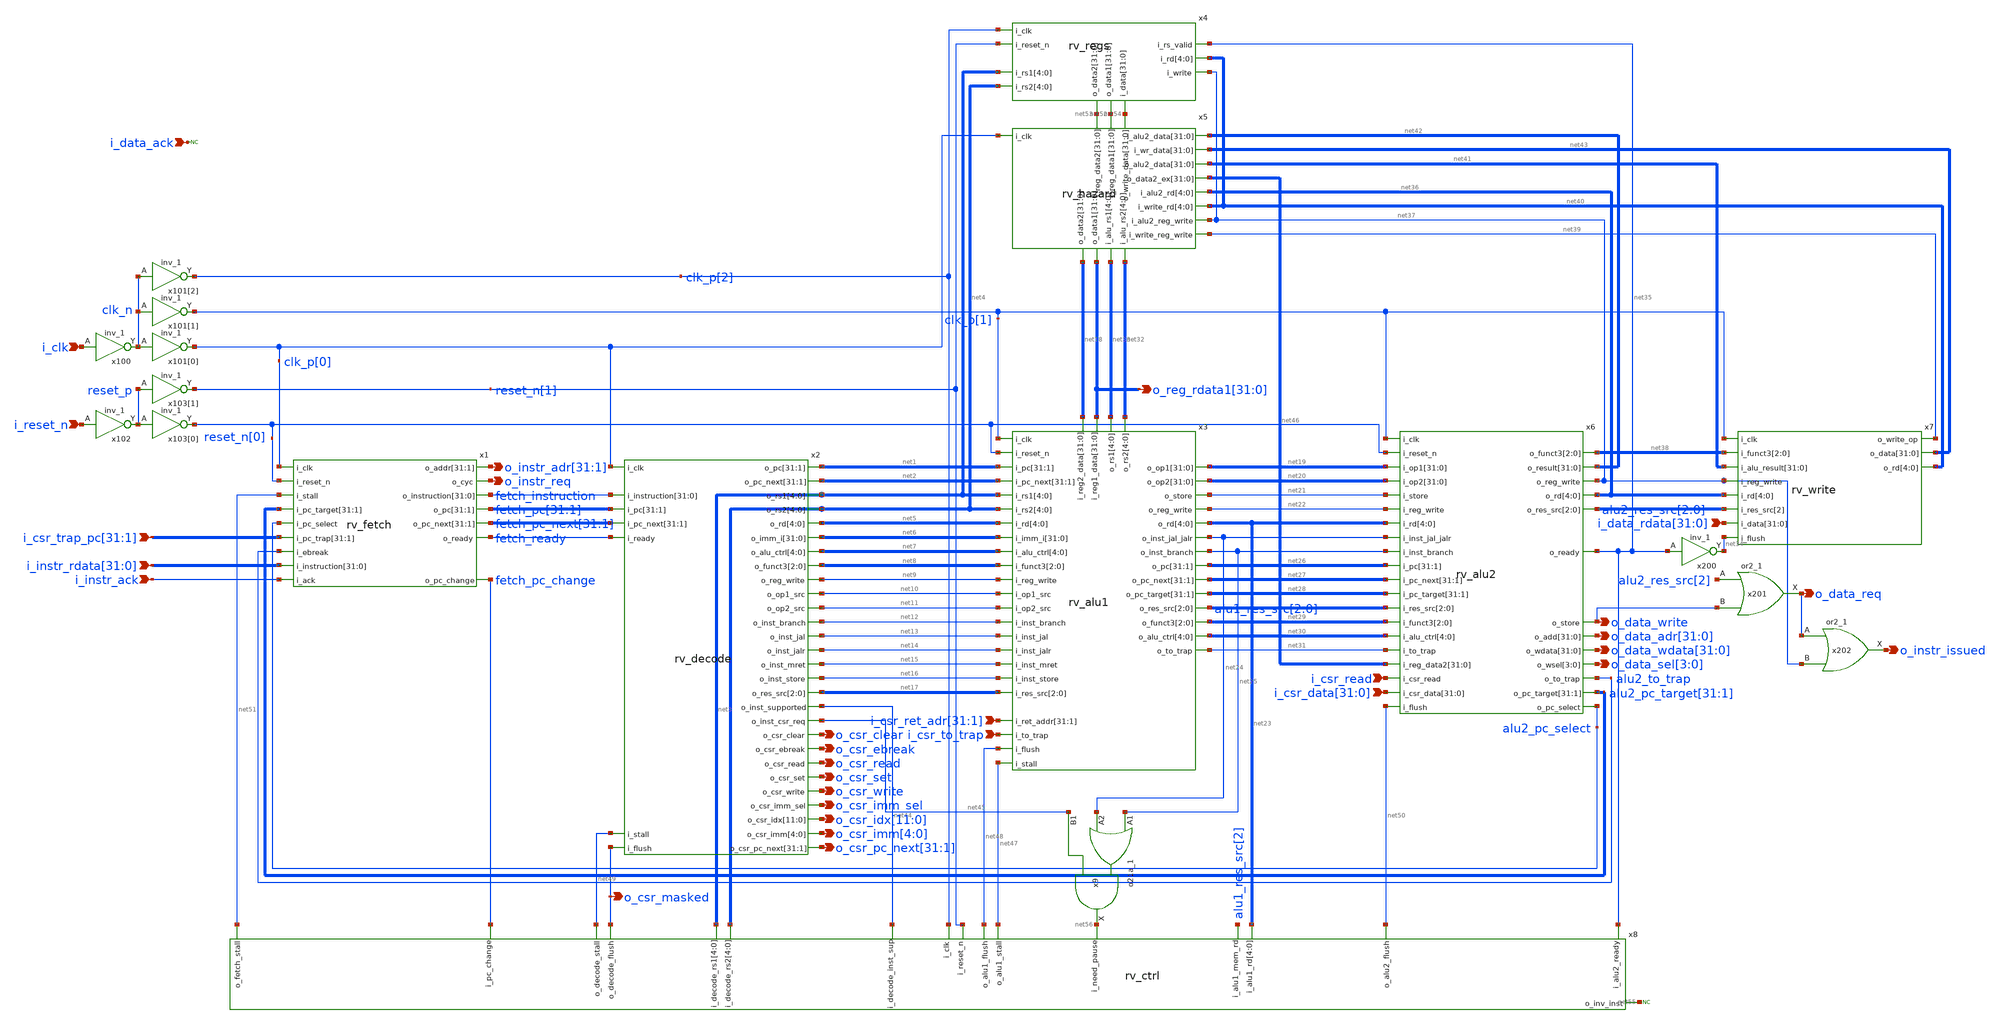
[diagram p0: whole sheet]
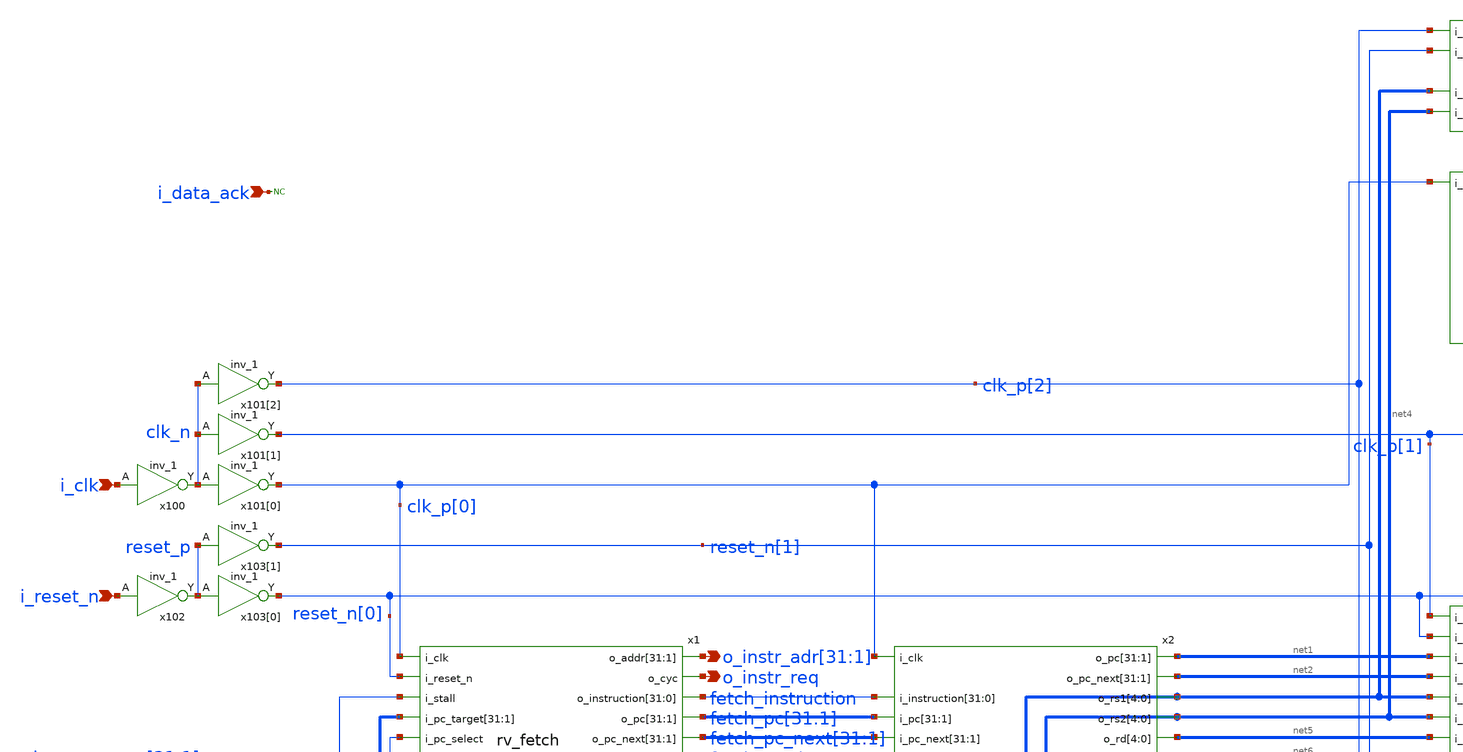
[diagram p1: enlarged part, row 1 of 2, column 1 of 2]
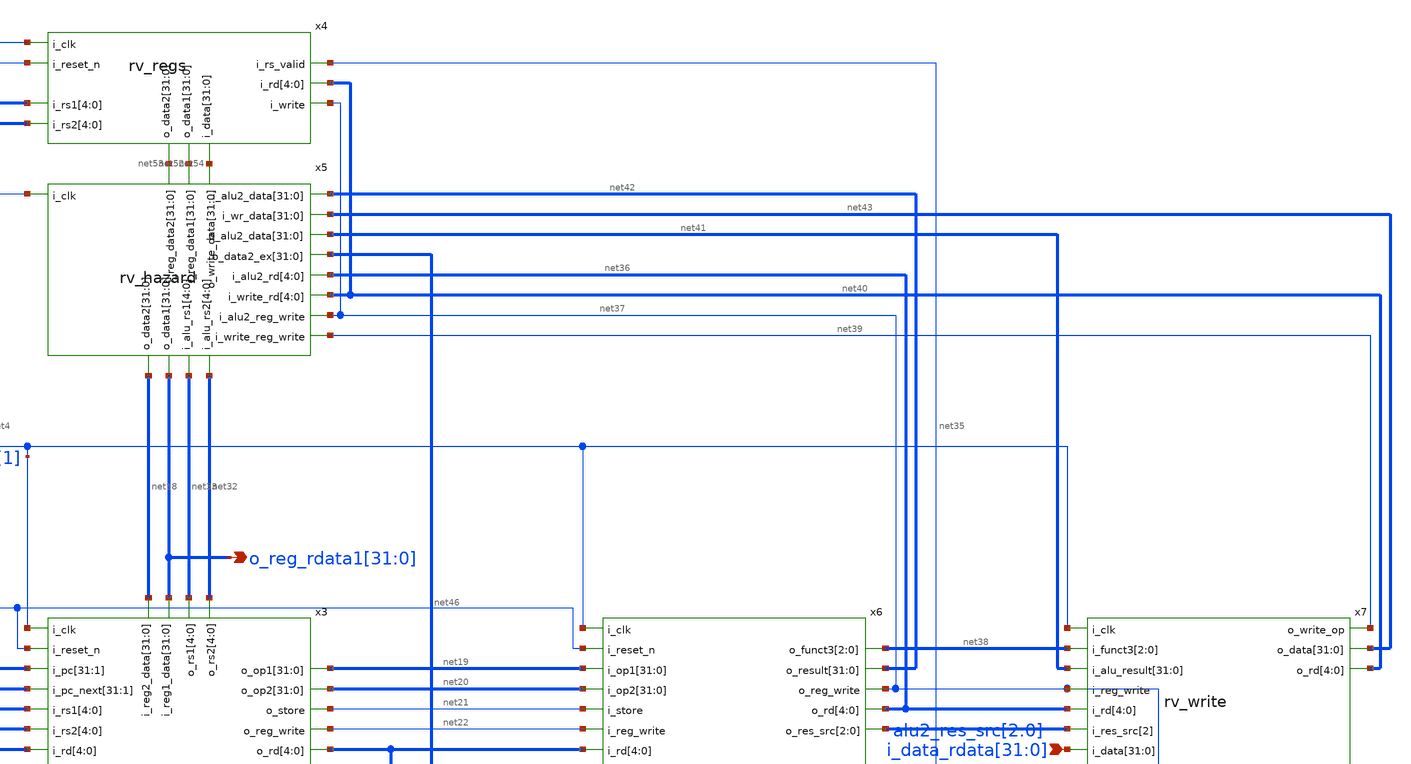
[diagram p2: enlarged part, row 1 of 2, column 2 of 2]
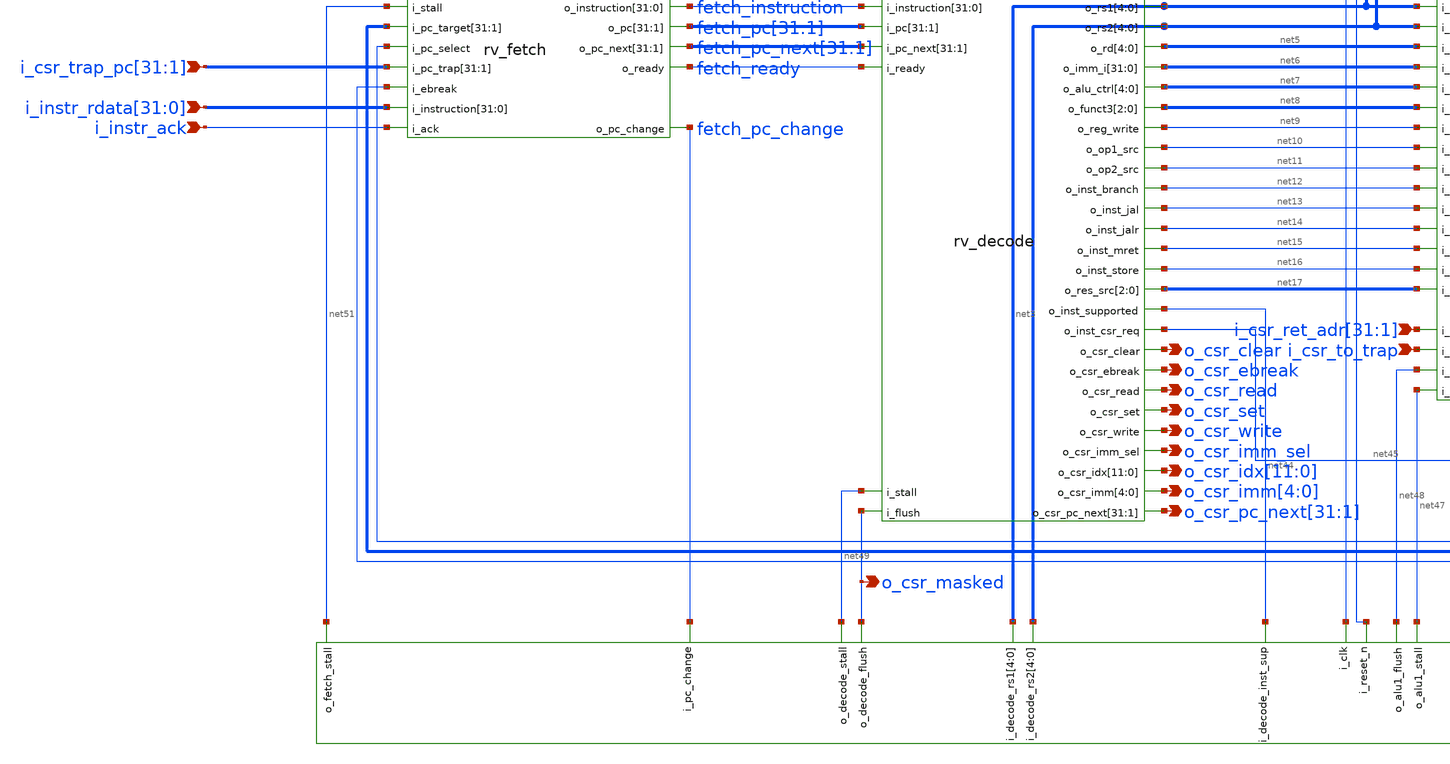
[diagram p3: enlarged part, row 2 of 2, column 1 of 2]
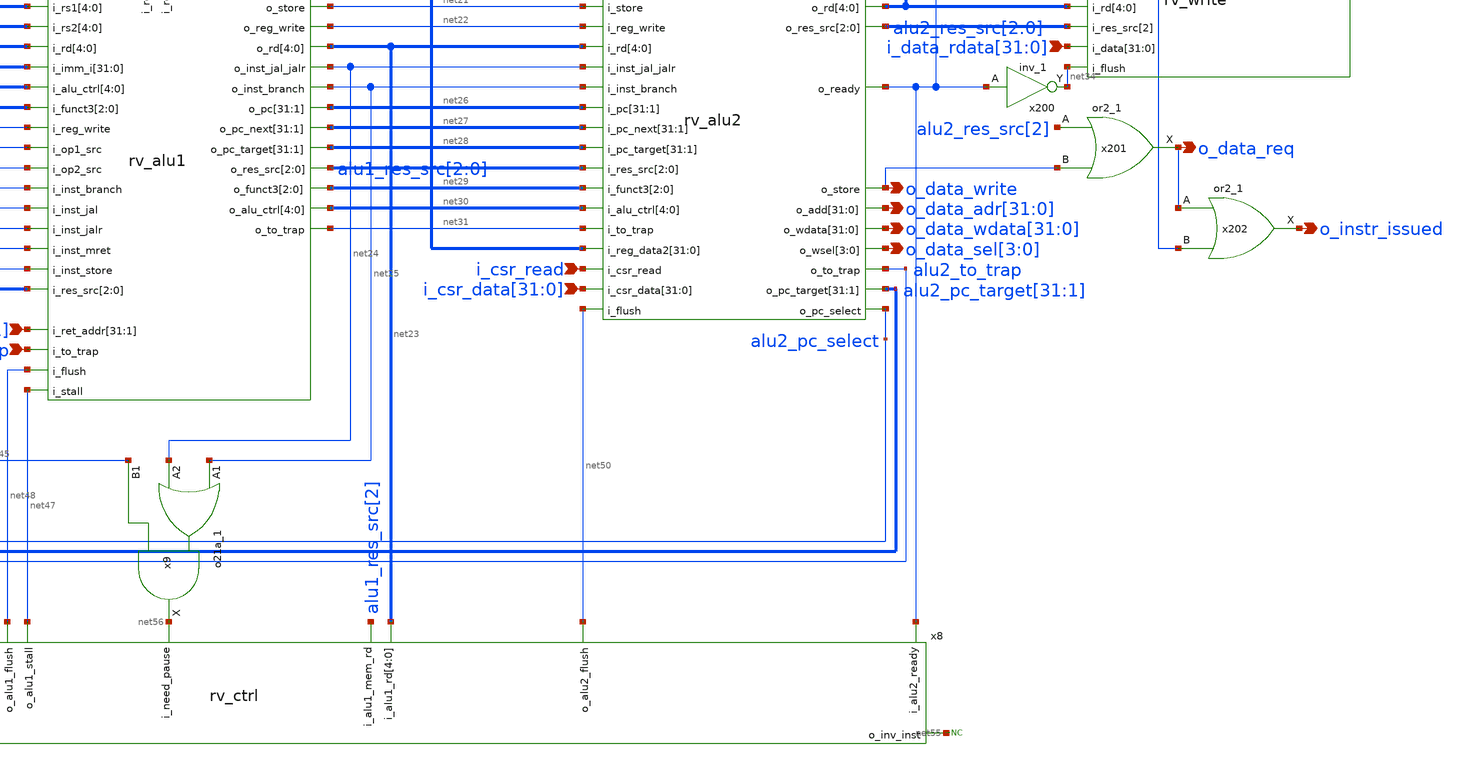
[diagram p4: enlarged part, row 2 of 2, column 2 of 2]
** sch_path: blocks/rv_core/rv_core.sch
**.subckt rv_core i_clk i_reset_n i_csr_read o_csr_clear o_data_req
*+ o_data_wdata[31],o_data_wdata[30],o_data_wdata[29],o_data_wdata[28],o_data_wdata[27],o_data_wdata[26],o_data_wdata[25],o_data_wdata[24],o_data_wdata[23],o_data_wdata[22],o_data_wdata[21],o_data_wdata[20],o_data_wdata[19],o_data_wdata[18],o_data_wdata[17],o_data_wdata[16],o_data_wdata[15],o_data_wdata[14],o_data_wdata[13],o_data_wdata[12],o_data_wdata[11],o_data_wdata[10],o_data_wdata[9],o_data_wdata[8],o_data_wdata[7],o_data_wdata[6],o_data_wdata[5],o_data_wdata[4],o_data_wdata[3],o_data_wdata[2],o_data_wdata[1],o_data_wdata[0] o_instr_issued
*+ o_data_adr[31],o_data_adr[30],o_data_adr[29],o_data_adr[28],o_data_adr[27],o_data_adr[26],o_data_adr[25],o_data_adr[24],o_data_adr[23],o_data_adr[22],o_data_adr[21],o_data_adr[20],o_data_adr[19],o_data_adr[18],o_data_adr[17],o_data_adr[16],o_data_adr[15],o_data_adr[14],o_data_adr[13],o_data_adr[12],o_data_adr[11],o_data_adr[10],o_data_adr[9],o_data_adr[8],o_data_adr[7],o_data_adr[6],o_data_adr[5],o_data_adr[4],o_data_adr[3],o_data_adr[2],o_data_adr[1],o_data_adr[0] o_data_sel[3],o_data_sel[2],o_data_sel[1],o_data_sel[0]
*+ i_csr_data[31],i_csr_data[30],i_csr_data[29],i_csr_data[28],i_csr_data[27],i_csr_data[26],i_csr_data[25],i_csr_data[24],i_csr_data[23],i_csr_data[22],i_csr_data[21],i_csr_data[20],i_csr_data[19],i_csr_data[18],i_csr_data[17],i_csr_data[16],i_csr_data[15],i_csr_data[14],i_csr_data[13],i_csr_data[12],i_csr_data[11],i_csr_data[10],i_csr_data[9],i_csr_data[8],i_csr_data[7],i_csr_data[6],i_csr_data[5],i_csr_data[4],i_csr_data[3],i_csr_data[2],i_csr_data[1],i_csr_data[0] i_csr_to_trap o_csr_ebreak o_csr_read o_csr_set o_csr_write o_csr_imm_sel
*+ i_csr_ret_adr[31],i_csr_ret_adr[30],i_csr_ret_adr[29],i_csr_ret_adr[28],i_csr_ret_adr[27],i_csr_ret_adr[26],i_csr_ret_adr[25],i_csr_ret_adr[24],i_csr_ret_adr[23],i_csr_ret_adr[22],i_csr_ret_adr[21],i_csr_ret_adr[20],i_csr_ret_adr[19],i_csr_ret_adr[18],i_csr_ret_adr[17],i_csr_ret_adr[16],i_csr_ret_adr[15],i_csr_ret_adr[14],i_csr_ret_adr[13],i_csr_ret_adr[12],i_csr_ret_adr[11],i_csr_ret_adr[10],i_csr_ret_adr[9],i_csr_ret_adr[8],i_csr_ret_adr[7],i_csr_ret_adr[6],i_csr_ret_adr[5],i_csr_ret_adr[4],i_csr_ret_adr[3],i_csr_ret_adr[2],i_csr_ret_adr[1]
*+ i_csr_trap_pc[31],i_csr_trap_pc[30],i_csr_trap_pc[29],i_csr_trap_pc[28],i_csr_trap_pc[27],i_csr_trap_pc[26],i_csr_trap_pc[25],i_csr_trap_pc[24],i_csr_trap_pc[23],i_csr_trap_pc[22],i_csr_trap_pc[21],i_csr_trap_pc[20],i_csr_trap_pc[19],i_csr_trap_pc[18],i_csr_trap_pc[17],i_csr_trap_pc[16],i_csr_trap_pc[15],i_csr_trap_pc[14],i_csr_trap_pc[13],i_csr_trap_pc[12],i_csr_trap_pc[11],i_csr_trap_pc[10],i_csr_trap_pc[9],i_csr_trap_pc[8],i_csr_trap_pc[7],i_csr_trap_pc[6],i_csr_trap_pc[5],i_csr_trap_pc[4],i_csr_trap_pc[3],i_csr_trap_pc[2],i_csr_trap_pc[1]
*+ o_csr_idx[11],o_csr_idx[10],o_csr_idx[9],o_csr_idx[8],o_csr_idx[7],o_csr_idx[6],o_csr_idx[5],o_csr_idx[4],o_csr_idx[3],o_csr_idx[2],o_csr_idx[1],o_csr_idx[0] o_csr_imm[4],o_csr_imm[3],o_csr_imm[2],o_csr_imm[1],o_csr_imm[0]
*+ o_csr_pc_next[31],o_csr_pc_next[30],o_csr_pc_next[29],o_csr_pc_next[28],o_csr_pc_next[27],o_csr_pc_next[26],o_csr_pc_next[25],o_csr_pc_next[24],o_csr_pc_next[23],o_csr_pc_next[22],o_csr_pc_next[21],o_csr_pc_next[20],o_csr_pc_next[19],o_csr_pc_next[18],o_csr_pc_next[17],o_csr_pc_next[16],o_csr_pc_next[15],o_csr_pc_next[14],o_csr_pc_next[13],o_csr_pc_next[12],o_csr_pc_next[11],o_csr_pc_next[10],o_csr_pc_next[9],o_csr_pc_next[8],o_csr_pc_next[7],o_csr_pc_next[6],o_csr_pc_next[5],o_csr_pc_next[4],o_csr_pc_next[3],o_csr_pc_next[2],o_csr_pc_next[1]
*+ o_reg_rdata1[31],o_reg_rdata1[30],o_reg_rdata1[29],o_reg_rdata1[28],o_reg_rdata1[27],o_reg_rdata1[26],o_reg_rdata1[25],o_reg_rdata1[24],o_reg_rdata1[23],o_reg_rdata1[22],o_reg_rdata1[21],o_reg_rdata1[20],o_reg_rdata1[19],o_reg_rdata1[18],o_reg_rdata1[17],o_reg_rdata1[16],o_reg_rdata1[15],o_reg_rdata1[14],o_reg_rdata1[13],o_reg_rdata1[12],o_reg_rdata1[11],o_reg_rdata1[10],o_reg_rdata1[9],o_reg_rdata1[8],o_reg_rdata1[7],o_reg_rdata1[6],o_reg_rdata1[5],o_reg_rdata1[4],o_reg_rdata1[3],o_reg_rdata1[2],o_reg_rdata1[1],o_reg_rdata1[0] i_data_ack o_data_write
*+ i_data_rdata[31],i_data_rdata[30],i_data_rdata[29],i_data_rdata[28],i_data_rdata[27],i_data_rdata[26],i_data_rdata[25],i_data_rdata[24],i_data_rdata[23],i_data_rdata[22],i_data_rdata[21],i_data_rdata[20],i_data_rdata[19],i_data_rdata[18],i_data_rdata[17],i_data_rdata[16],i_data_rdata[15],i_data_rdata[14],i_data_rdata[13],i_data_rdata[12],i_data_rdata[11],i_data_rdata[10],i_data_rdata[9],i_data_rdata[8],i_data_rdata[7],i_data_rdata[6],i_data_rdata[5],i_data_rdata[4],i_data_rdata[3],i_data_rdata[2],i_data_rdata[1],i_data_rdata[0] i_instr_ack o_instr_req
*+ i_instr_rdata[31],i_instr_rdata[30],i_instr_rdata[29],i_instr_rdata[28],i_instr_rdata[27],i_instr_rdata[26],i_instr_rdata[25],i_instr_rdata[24],i_instr_rdata[23],i_instr_rdata[22],i_instr_rdata[21],i_instr_rdata[20],i_instr_rdata[19],i_instr_rdata[18],i_instr_rdata[17],i_instr_rdata[16],i_instr_rdata[15],i_instr_rdata[14],i_instr_rdata[13],i_instr_rdata[12],i_instr_rdata[11],i_instr_rdata[10],i_instr_rdata[9],i_instr_rdata[8],i_instr_rdata[7],i_instr_rdata[6],i_instr_rdata[5],i_instr_rdata[4],i_instr_rdata[3],i_instr_rdata[2],i_instr_rdata[1],i_instr_rdata[0]
*+ o_instr_adr[31],o_instr_adr[30],o_instr_adr[29],o_instr_adr[28],o_instr_adr[27],o_instr_adr[26],o_instr_adr[25],o_instr_adr[24],o_instr_adr[23],o_instr_adr[22],o_instr_adr[21],o_instr_adr[20],o_instr_adr[19],o_instr_adr[18],o_instr_adr[17],o_instr_adr[16],o_instr_adr[15],o_instr_adr[14],o_instr_adr[13],o_instr_adr[12],o_instr_adr[11],o_instr_adr[10],o_instr_adr[9],o_instr_adr[8],o_instr_adr[7],o_instr_adr[6],o_instr_adr[5],o_instr_adr[4],o_instr_adr[3],o_instr_adr[2],o_instr_adr[1] o_csr_masked
*.ipin i_clk
*.ipin i_reset_n
*.ipin i_csr_read
*.opin o_csr_clear
*.opin o_data_req
*.opin
*+ o_data_wdata[31],o_data_wdata[30],o_data_wdata[29],o_data_wdata[28],o_data_wdata[27],o_data_wdata[26],o_data_wdata[25],o_data_wdata[24],o_data_wdata[23],o_data_wdata[22],o_data_wdata[21],o_data_wdata[20],o_data_wdata[19],o_data_wdata[18],o_data_wdata[17],o_data_wdata[16],o_data_wdata[15],o_data_wdata[14],o_data_wdata[13],o_data_wdata[12],o_data_wdata[11],o_data_wdata[10],o_data_wdata[9],o_data_wdata[8],o_data_wdata[7],o_data_wdata[6],o_data_wdata[5],o_data_wdata[4],o_data_wdata[3],o_data_wdata[2],o_data_wdata[1],o_data_wdata[0]
*.opin o_instr_issued
*.opin
*+ o_data_adr[31],o_data_adr[30],o_data_adr[29],o_data_adr[28],o_data_adr[27],o_data_adr[26],o_data_adr[25],o_data_adr[24],o_data_adr[23],o_data_adr[22],o_data_adr[21],o_data_adr[20],o_data_adr[19],o_data_adr[18],o_data_adr[17],o_data_adr[16],o_data_adr[15],o_data_adr[14],o_data_adr[13],o_data_adr[12],o_data_adr[11],o_data_adr[10],o_data_adr[9],o_data_adr[8],o_data_adr[7],o_data_adr[6],o_data_adr[5],o_data_adr[4],o_data_adr[3],o_data_adr[2],o_data_adr[1],o_data_adr[0]
*.opin o_data_sel[3],o_data_sel[2],o_data_sel[1],o_data_sel[0]
*.ipin
*+ i_csr_data[31],i_csr_data[30],i_csr_data[29],i_csr_data[28],i_csr_data[27],i_csr_data[26],i_csr_data[25],i_csr_data[24],i_csr_data[23],i_csr_data[22],i_csr_data[21],i_csr_data[20],i_csr_data[19],i_csr_data[18],i_csr_data[17],i_csr_data[16],i_csr_data[15],i_csr_data[14],i_csr_data[13],i_csr_data[12],i_csr_data[11],i_csr_data[10],i_csr_data[9],i_csr_data[8],i_csr_data[7],i_csr_data[6],i_csr_data[5],i_csr_data[4],i_csr_data[3],i_csr_data[2],i_csr_data[1],i_csr_data[0]
*.ipin i_csr_to_trap
*.opin o_csr_ebreak
*.opin o_csr_read
*.opin o_csr_set
*.opin o_csr_write
*.opin o_csr_imm_sel
*.ipin
*+ i_csr_ret_adr[31],i_csr_ret_adr[30],i_csr_ret_adr[29],i_csr_ret_adr[28],i_csr_ret_adr[27],i_csr_ret_adr[26],i_csr_ret_adr[25],i_csr_ret_adr[24],i_csr_ret_adr[23],i_csr_ret_adr[22],i_csr_ret_adr[21],i_csr_ret_adr[20],i_csr_ret_adr[19],i_csr_ret_adr[18],i_csr_ret_adr[17],i_csr_ret_adr[16],i_csr_ret_adr[15],i_csr_ret_adr[14],i_csr_ret_adr[13],i_csr_ret_adr[12],i_csr_ret_adr[11],i_csr_ret_adr[10],i_csr_ret_adr[9],i_csr_ret_adr[8],i_csr_ret_adr[7],i_csr_ret_adr[6],i_csr_ret_adr[5],i_csr_ret_adr[4],i_csr_ret_adr[3],i_csr_ret_adr[2],i_csr_ret_adr[1]
*.ipin
*+ i_csr_trap_pc[31],i_csr_trap_pc[30],i_csr_trap_pc[29],i_csr_trap_pc[28],i_csr_trap_pc[27],i_csr_trap_pc[26],i_csr_trap_pc[25],i_csr_trap_pc[24],i_csr_trap_pc[23],i_csr_trap_pc[22],i_csr_trap_pc[21],i_csr_trap_pc[20],i_csr_trap_pc[19],i_csr_trap_pc[18],i_csr_trap_pc[17],i_csr_trap_pc[16],i_csr_trap_pc[15],i_csr_trap_pc[14],i_csr_trap_pc[13],i_csr_trap_pc[12],i_csr_trap_pc[11],i_csr_trap_pc[10],i_csr_trap_pc[9],i_csr_trap_pc[8],i_csr_trap_pc[7],i_csr_trap_pc[6],i_csr_trap_pc[5],i_csr_trap_pc[4],i_csr_trap_pc[3],i_csr_trap_pc[2],i_csr_trap_pc[1]
*.opin
*+ o_csr_idx[11],o_csr_idx[10],o_csr_idx[9],o_csr_idx[8],o_csr_idx[7],o_csr_idx[6],o_csr_idx[5],o_csr_idx[4],o_csr_idx[3],o_csr_idx[2],o_csr_idx[1],o_csr_idx[0]
*.opin o_csr_imm[4],o_csr_imm[3],o_csr_imm[2],o_csr_imm[1],o_csr_imm[0]
*.opin
*+ o_csr_pc_next[31],o_csr_pc_next[30],o_csr_pc_next[29],o_csr_pc_next[28],o_csr_pc_next[27],o_csr_pc_next[26],o_csr_pc_next[25],o_csr_pc_next[24],o_csr_pc_next[23],o_csr_pc_next[22],o_csr_pc_next[21],o_csr_pc_next[20],o_csr_pc_next[19],o_csr_pc_next[18],o_csr_pc_next[17],o_csr_pc_next[16],o_csr_pc_next[15],o_csr_pc_next[14],o_csr_pc_next[13],o_csr_pc_next[12],o_csr_pc_next[11],o_csr_pc_next[10],o_csr_pc_next[9],o_csr_pc_next[8],o_csr_pc_next[7],o_csr_pc_next[6],o_csr_pc_next[5],o_csr_pc_next[4],o_csr_pc_next[3],o_csr_pc_next[2],o_csr_pc_next[1]
*.opin
*+ o_reg_rdata1[31],o_reg_rdata1[30],o_reg_rdata1[29],o_reg_rdata1[28],o_reg_rdata1[27],o_reg_rdata1[26],o_reg_rdata1[25],o_reg_rdata1[24],o_reg_rdata1[23],o_reg_rdata1[22],o_reg_rdata1[21],o_reg_rdata1[20],o_reg_rdata1[19],o_reg_rdata1[18],o_reg_rdata1[17],o_reg_rdata1[16],o_reg_rdata1[15],o_reg_rdata1[14],o_reg_rdata1[13],o_reg_rdata1[12],o_reg_rdata1[11],o_reg_rdata1[10],o_reg_rdata1[9],o_reg_rdata1[8],o_reg_rdata1[7],o_reg_rdata1[6],o_reg_rdata1[5],o_reg_rdata1[4],o_reg_rdata1[3],o_reg_rdata1[2],o_reg_rdata1[1],o_reg_rdata1[0]
*.ipin i_data_ack
*.opin o_data_write
*.ipin
*+ i_data_rdata[31],i_data_rdata[30],i_data_rdata[29],i_data_rdata[28],i_data_rdata[27],i_data_rdata[26],i_data_rdata[25],i_data_rdata[24],i_data_rdata[23],i_data_rdata[22],i_data_rdata[21],i_data_rdata[20],i_data_rdata[19],i_data_rdata[18],i_data_rdata[17],i_data_rdata[16],i_data_rdata[15],i_data_rdata[14],i_data_rdata[13],i_data_rdata[12],i_data_rdata[11],i_data_rdata[10],i_data_rdata[9],i_data_rdata[8],i_data_rdata[7],i_data_rdata[6],i_data_rdata[5],i_data_rdata[4],i_data_rdata[3],i_data_rdata[2],i_data_rdata[1],i_data_rdata[0]
*.ipin i_instr_ack
*.opin o_instr_req
*.ipin
*+ i_instr_rdata[31],i_instr_rdata[30],i_instr_rdata[29],i_instr_rdata[28],i_instr_rdata[27],i_instr_rdata[26],i_instr_rdata[25],i_instr_rdata[24],i_instr_rdata[23],i_instr_rdata[22],i_instr_rdata[21],i_instr_rdata[20],i_instr_rdata[19],i_instr_rdata[18],i_instr_rdata[17],i_instr_rdata[16],i_instr_rdata[15],i_instr_rdata[14],i_instr_rdata[13],i_instr_rdata[12],i_instr_rdata[11],i_instr_rdata[10],i_instr_rdata[9],i_instr_rdata[8],i_instr_rdata[7],i_instr_rdata[6],i_instr_rdata[5],i_instr_rdata[4],i_instr_rdata[3],i_instr_rdata[2],i_instr_rdata[1],i_instr_rdata[0]
*.opin
*+ o_instr_adr[31],o_instr_adr[30],o_instr_adr[29],o_instr_adr[28],o_instr_adr[27],o_instr_adr[26],o_instr_adr[25],o_instr_adr[24],o_instr_adr[23],o_instr_adr[22],o_instr_adr[21],o_instr_adr[20],o_instr_adr[19],o_instr_adr[18],o_instr_adr[17],o_instr_adr[16],o_instr_adr[15],o_instr_adr[14],o_instr_adr[13],o_instr_adr[12],o_instr_adr[11],o_instr_adr[10],o_instr_adr[9],o_instr_adr[8],o_instr_adr[7],o_instr_adr[6],o_instr_adr[5],o_instr_adr[4],o_instr_adr[3],o_instr_adr[2],o_instr_adr[1]
*.opin o_csr_masked
x1 fetch_pc_change clk_p[0] reset_n[0] o_instr_adr[31] o_instr_adr[30] o_instr_adr[29]
+ o_instr_adr[28] o_instr_adr[27] o_instr_adr[26] o_instr_adr[25] o_instr_adr[24] o_instr_adr[23] o_instr_adr[22]
+ o_instr_adr[21] o_instr_adr[20] o_instr_adr[19] o_instr_adr[18] o_instr_adr[17] o_instr_adr[16] o_instr_adr[15]
+ o_instr_adr[14] o_instr_adr[13] o_instr_adr[12] o_instr_adr[11] o_instr_adr[10] o_instr_adr[9] o_instr_adr[8]
+ o_instr_adr[7] o_instr_adr[6] o_instr_adr[5] o_instr_adr[4] o_instr_adr[3] o_instr_adr[2] o_instr_adr[1]
+ o_instr_req net51 fetch_instruction fetch_instruction fetch_instruction fetch_instruction fetch_instruction
+ fetch_instruction fetch_instruction fetch_instruction fetch_instruction fetch_instruction fetch_instruction
+ fetch_instruction fetch_instruction fetch_instruction fetch_instruction fetch_instruction fetch_instruction
+ fetch_instruction fetch_instruction fetch_instruction fetch_instruction fetch_instruction fetch_instruction
+ fetch_instruction fetch_instruction fetch_instruction fetch_instruction fetch_instruction fetch_instruction
+ fetch_instruction fetch_instruction fetch_instruction alu2_pc_target[31] alu2_pc_target[30] alu2_pc_target[29]
+ alu2_pc_target[28] alu2_pc_target[27] alu2_pc_target[26] alu2_pc_target[25] alu2_pc_target[24] alu2_pc_target[23]
+ alu2_pc_target[22] alu2_pc_target[21] alu2_pc_target[20] alu2_pc_target[19] alu2_pc_target[18] alu2_pc_target[17]
+ alu2_pc_target[16] alu2_pc_target[15] alu2_pc_target[14] alu2_pc_target[13] alu2_pc_target[12] alu2_pc_target[11]
+ alu2_pc_target[10] alu2_pc_target[9] alu2_pc_target[8] alu2_pc_target[7] alu2_pc_target[6] alu2_pc_target[5]
+ alu2_pc_target[4] alu2_pc_target[3] alu2_pc_target[2] alu2_pc_target[1] alu2_pc_select fetch_pc[31] fetch_pc[30]
+ fetch_pc[29] fetch_pc[28] fetch_pc[27] fetch_pc[26] fetch_pc[25] fetch_pc[24] fetch_pc[23] fetch_pc[22]
+ fetch_pc[21] fetch_pc[20] fetch_pc[19] fetch_pc[18] fetch_pc[17] fetch_pc[16] fetch_pc[15] fetch_pc[14]
+ fetch_pc[13] fetch_pc[12] fetch_pc[11] fetch_pc[10] fetch_pc[9] fetch_pc[8] fetch_pc[7] fetch_pc[6] fetch_pc[5]
+ fetch_pc[4] fetch_pc[3] fetch_pc[2] fetch_pc[1] fetch_pc_next[31] fetch_pc_next[30] fetch_pc_next[29]
+ fetch_pc_next[28] fetch_pc_next[27] fetch_pc_next[26] fetch_pc_next[25] fetch_pc_next[24] fetch_pc_next[23]
+ fetch_pc_next[22] fetch_pc_next[21] fetch_pc_next[20] fetch_pc_next[19] fetch_pc_next[18] fetch_pc_next[17]
+ fetch_pc_next[16] fetch_pc_next[15] fetch_pc_next[14] fetch_pc_next[13] fetch_pc_next[12] fetch_pc_next[11]
+ fetch_pc_next[10] fetch_pc_next[9] fetch_pc_next[8] fetch_pc_next[7] fetch_pc_next[6] fetch_pc_next[5]
+ fetch_pc_next[4] fetch_pc_next[3] fetch_pc_next[2] fetch_pc_next[1] i_csr_trap_pc[31] i_csr_trap_pc[30]
+ i_csr_trap_pc[29] i_csr_trap_pc[28] i_csr_trap_pc[27] i_csr_trap_pc[26] i_csr_trap_pc[25] i_csr_trap_pc[24]
+ i_csr_trap_pc[23] i_csr_trap_pc[22] i_csr_trap_pc[21] i_csr_trap_pc[20] i_csr_trap_pc[19] i_csr_trap_pc[18]
+ i_csr_trap_pc[17] i_csr_trap_pc[16] i_csr_trap_pc[15] i_csr_trap_pc[14] i_csr_trap_pc[13] i_csr_trap_pc[12]
+ i_csr_trap_pc[11] i_csr_trap_pc[10] i_csr_trap_pc[9] i_csr_trap_pc[8] i_csr_trap_pc[7] i_csr_trap_pc[6]
+ i_csr_trap_pc[5] i_csr_trap_pc[4] i_csr_trap_pc[3] i_csr_trap_pc[2] i_csr_trap_pc[1] fetch_ready alu2_to_trap
+ i_instr_rdata[31] i_instr_rdata[30] i_instr_rdata[29] i_instr_rdata[28] i_instr_rdata[27] i_instr_rdata[26]
+ i_instr_rdata[25] i_instr_rdata[24] i_instr_rdata[23] i_instr_rdata[22] i_instr_rdata[21] i_instr_rdata[20]
+ i_instr_rdata[19] i_instr_rdata[18] i_instr_rdata[17] i_instr_rdata[16] i_instr_rdata[15] i_instr_rdata[14]
+ i_instr_rdata[13] i_instr_rdata[12] i_instr_rdata[11] i_instr_rdata[10] i_instr_rdata[9] i_instr_rdata[8]
+ i_instr_rdata[7] i_instr_rdata[6] i_instr_rdata[5] i_instr_rdata[4] i_instr_rdata[3] i_instr_rdata[2]
+ i_instr_rdata[1] i_instr_rdata[0] i_instr_ack rv_fetch
x100 i_clk VSS VSS VCC VCC clk_n sky130_fd_sc_hs__inv_1
x102 i_reset_n VSS VSS VCC VCC reset_p sky130_fd_sc_hs__inv_1
x103[0] reset_p VSS VSS VCC VCC reset_n[0] sky130_fd_sc_hs__inv_1
x101[2] clk_n VSS VSS VCC VCC clk_p[2] sky130_fd_sc_hs__inv_1
x101[1] clk_n VSS VSS VCC VCC clk_p[1] sky130_fd_sc_hs__inv_1
x101[0] clk_n VSS VSS VCC VCC clk_p[0] sky130_fd_sc_hs__inv_1
x103[1] reset_p VSS VSS VCC VCC reset_n[1] sky130_fd_sc_hs__inv_1
x2 net1[30] net1[29] net1[28] net1[27] net1[26] net1[25] net1[24] net1[23] net1[22] net1[21]
+ net1[20] net1[19] net1[18] net1[17] net1[16] net1[15] net1[14] net1[13] net1[12] net1[11] net1[10] net1[9]
+ net1[8] net1[7] net1[6] net1[5] net1[4] net1[3] net1[2] net1[1] net1[0] clk_p[0] net49 net2[30] net2[29]
+ net2[28] net2[27] net2[26] net2[25] net2[24] net2[23] net2[22] net2[21] net2[20] net2[19] net2[18] net2[17]
+ net2[16] net2[15] net2[14] net2[13] net2[12] net2[11] net2[10] net2[9] net2[8] net2[7] net2[6] net2[5]
+ net2[4] net2[3] net2[2] net2[1] net2[0] o_csr_masked net3[4] net3[3] net3[2] net3[1] net3[0]
+ fetch_instruction fetch_instruction fetch_instruction fetch_instruction fetch_instruction fetch_instruction
+ fetch_instruction fetch_instruction fetch_instruction fetch_instruction fetch_instruction fetch_instruction
+ fetch_instruction fetch_instruction fetch_instruction fetch_instruction fetch_instruction fetch_instruction
+ fetch_instruction fetch_instruction fetch_instruction fetch_instruction fetch_instruction fetch_instruction
+ fetch_instruction fetch_instruction fetch_instruction fetch_instruction fetch_instruction fetch_instruction
+ fetch_instruction fetch_instruction net4[4] net4[3] net4[2] net4[1] net4[0] net5[4] net5[3] net5[2] net5[1] net5[0]
+ fetch_pc[31] fetch_pc[30] fetch_pc[29] fetch_pc[28] fetch_pc[27] fetch_pc[26] fetch_pc[25] fetch_pc[24]
+ fetch_pc[23] fetch_pc[22] fetch_pc[21] fetch_pc[20] fetch_pc[19] fetch_pc[18] fetch_pc[17] fetch_pc[16]
+ fetch_pc[15] fetch_pc[14] fetch_pc[13] fetch_pc[12] fetch_pc[11] fetch_pc[10] fetch_pc[9] fetch_pc[8]
+ fetch_pc[7] fetch_pc[6] fetch_pc[5] fetch_pc[4] fetch_pc[3] fetch_pc[2] fetch_pc[1] net6[31] net6[30] net6[29]
+ net6[28] net6[27] net6[26] net6[25] net6[24] net6[23] net6[22] net6[21] net6[20] net6[19] net6[18] net6[17]
+ net6[16] net6[15] net6[14] net6[13] net6[12] net6[11] net6[10] net6[9] net6[8] net6[7] net6[6] net6[5]
+ net6[4] net6[3] net6[2] net6[1] net6[0] fetch_pc_next[31] fetch_pc_next[30] fetch_pc_next[29]
+ fetch_pc_next[28] fetch_pc_next[27] fetch_pc_next[26] fetch_pc_next[25] fetch_pc_next[24] fetch_pc_next[23]
+ fetch_pc_next[22] fetch_pc_next[21] fetch_pc_next[20] fetch_pc_next[19] fetch_pc_next[18] fetch_pc_next[17]
+ fetch_pc_next[16] fetch_pc_next[15] fetch_pc_next[14] fetch_pc_next[13] fetch_pc_next[12] fetch_pc_next[11]
+ fetch_pc_next[10] fetch_pc_next[9] fetch_pc_next[8] fetch_pc_next[7] fetch_pc_next[6] fetch_pc_next[5]
+ fetch_pc_next[4] fetch_pc_next[3] fetch_pc_next[2] fetch_pc_next[1] fetch_ready net7[4] net7[3] net7[2] net7[1]
+ net7[0] net8[2] net8[1] net8[0] net9 net10 net11 net12 net45 net13 net14 net15 net16 net44 net17[2]
+ net17[1] net17[0] o_csr_clear o_csr_ebreak o_csr_read o_csr_set o_csr_write o_csr_imm_sel o_csr_idx[11]
+ o_csr_idx[10] o_csr_idx[9] o_csr_idx[8] o_csr_idx[7] o_csr_idx[6] o_csr_idx[5] o_csr_idx[4] o_csr_idx[3]
+ o_csr_idx[2] o_csr_idx[1] o_csr_idx[0] o_csr_imm[4] o_csr_imm[3] o_csr_imm[2] o_csr_imm[1] o_csr_imm[0]
+ o_csr_pc_next[31] o_csr_pc_next[30] o_csr_pc_next[29] o_csr_pc_next[28] o_csr_pc_next[27] o_csr_pc_next[26]
+ o_csr_pc_next[25] o_csr_pc_next[24] o_csr_pc_next[23] o_csr_pc_next[22] o_csr_pc_next[21] o_csr_pc_next[20]
+ o_csr_pc_next[19] o_csr_pc_next[18] o_csr_pc_next[17] o_csr_pc_next[16] o_csr_pc_next[15] o_csr_pc_next[14]
+ o_csr_pc_next[13] o_csr_pc_next[12] o_csr_pc_next[11] o_csr_pc_next[10] o_csr_pc_next[9] o_csr_pc_next[8]
+ o_csr_pc_next[7] o_csr_pc_next[6] o_csr_pc_next[5] o_csr_pc_next[4] o_csr_pc_next[3] o_csr_pc_next[2]
+ o_csr_pc_next[1] rv_decode
x3 clk_p[1] net19[31] net19[30] net19[29] net19[28] net19[27] net19[26] net19[25] net19[24]
+ net19[23] net19[22] net19[21] net19[20] net19[19] net19[18] net19[17] net19[16] net19[15] net19[14] net19[13]
+ net19[12] net19[11] net19[10] net19[9] net19[8] net19[7] net19[6] net19[5] net19[4] net19[3] net19[2]
+ net19[1] net19[0] reset_n[0] net20[31] net20[30] net20[29] net20[28] net20[27] net20[26] net20[25] net20[24]
+ net20[23] net20[22] net20[21] net20[20] net20[19] net20[18] net20[17] net20[16] net20[15] net20[14] net20[13]
+ net20[12] net20[11] net20[10] net20[9] net20[8] net20[7] net20[6] net20[5] net20[4] net20[3] net20[2]
+ net20[1] net20[0] net1[30] net1[29] net1[28] net1[27] net1[26] net1[25] net1[24] net1[23] net1[22] net1[21]
+ net1[20] net1[19] net1[18] net1[17] net1[16] net1[15] net1[14] net1[13] net1[12] net1[11] net1[10] net1[9]
+ net1[8] net1[7] net1[6] net1[5] net1[4] net1[3] net1[2] net1[1] net1[0] net21 net22 net2[30] net2[29]
+ net2[28] net2[27] net2[26] net2[25] net2[24] net2[23] net2[22] net2[21] net2[20] net2[19] net2[18] net2[17]
+ net2[16] net2[15] net2[14] net2[13] net2[12] net2[11] net2[10] net2[9] net2[8] net2[7] net2[6] net2[5]
+ net2[4] net2[3] net2[2] net2[1] net2[0] net33[4] net33[3] net33[2] net33[1] net33[0] net3[4] net3[3]
+ net3[2] net3[1] net3[0] net4[4] net4[3] net4[2] net4[1] net4[0] net32[4] net32[3] net32[2] net32[1]
+ net32[0] net5[4] net5[3] net5[2] net5[1] net5[0] net23[4] net23[3] net23[2] net23[1] net23[0] net6[31]
+ net6[30] net6[29] net6[28] net6[27] net6[26] net6[25] net6[24] net6[23] net6[22] net6[21] net6[20] net6[19]
+ net6[18] net6[17] net6[16] net6[15] net6[14] net6[13] net6[12] net6[11] net6[10] net6[9] net6[8] net6[7]
+ net6[6] net6[5] net6[4] net6[3] net6[2] net6[1] net6[0] net24 net7[4] net7[3] net7[2] net7[1] net7[0] net25
+ net8[2] net8[1] net8[0] net26[30] net26[29] net26[28] net26[27] net26[26] net26[25] net26[24] net26[23]
+ net26[22] net26[21] net26[20] net26[19] net26[18] net26[17] net26[16] net26[15] net26[14] net26[13] net26[12]
+ net26[11] net26[10] net26[9] net26[8] net26[7] net26[6] net26[5] net26[4] net26[3] net26[2] net26[1] net26[0]
+ net27[30] net27[29] net27[28] net27[27] net27[26] net27[25] net27[24] net27[23] net27[22] net27[21] net27[20]
+ net27[19] net27[18] net27[17] net27[16] net27[15] net27[14] net27[13] net27[12] net27[11] net27[10] net27[9]
+ net27[8] net27[7] net27[6] net27[5] net27[4] net27[3] net27[2] net27[1] net27[0] net9 net28[30] net28[29]
+ net28[28] net28[27] net28[26] net28[25] net28[24] net28[23] net28[22] net28[21] net28[20] net28[19] net28[18]
+ net28[17] net28[16] net28[15] net28[14] net28[13] net28[12] net28[11] net28[10] net28[9] net28[8] net28[7]
+ net28[6] net28[5] net28[4] net28[3] net28[2] net28[1] net28[0] net10 net11 alu1_res_src[2] alu1_res_src[1]
+ alu1_res_src[0] net12 net29[2] net29[1] net29[0] net30[4] net30[3] net30[2] net30[1] net30[0] net13 net31 net14
+ net15 net16 net17[2] net17[1] net17[0] o_reg_rdata1[31] o_reg_rdata1[30] o_reg_rdata1[29]
+ o_reg_rdata1[28] o_reg_rdata1[27] o_reg_rdata1[26] o_reg_rdata1[25] o_reg_rdata1[24] o_reg_rdata1[23]
+ o_reg_rdata1[22] o_reg_rdata1[21] o_reg_rdata1[20] o_reg_rdata1[19] o_reg_rdata1[18] o_reg_rdata1[17]
+ o_reg_rdata1[16] o_reg_rdata1[15] o_reg_rdata1[14] o_reg_rdata1[13] o_reg_rdata1[12] o_reg_rdata1[11]
+ o_reg_rdata1[10] o_reg_rdata1[9] o_reg_rdata1[8] o_reg_rdata1[7] o_reg_rdata1[6] o_reg_rdata1[5] o_reg_rdata1[4]
+ o_reg_rdata1[3] o_reg_rdata1[2] o_reg_rdata1[1] o_reg_rdata1[0] net18[31] net18[30] net18[29] net18[28] net18[27]
+ net18[26] net18[25] net18[24] net18[23] net18[22] net18[21] net18[20] net18[19] net18[18] net18[17] net18[16]
+ net18[15] net18[14] net18[13] net18[12] net18[11] net18[10] net18[9] net18[8] net18[7] net18[6] net18[5]
+ net18[4] net18[3] net18[2] net18[1] net18[0] i_csr_to_trap net48 net47 i_csr_ret_adr[31] i_csr_ret_adr[30]
+ i_csr_ret_adr[29] i_csr_ret_adr[28] i_csr_ret_adr[27] i_csr_ret_adr[26] i_csr_ret_adr[25] i_csr_ret_adr[24]
+ i_csr_ret_adr[23] i_csr_ret_adr[22] i_csr_ret_adr[21] i_csr_ret_adr[20] i_csr_ret_adr[19] i_csr_ret_adr[18]
+ i_csr_ret_adr[17] i_csr_ret_adr[16] i_csr_ret_adr[15] i_csr_ret_adr[14] i_csr_ret_adr[13] i_csr_ret_adr[12]
+ i_csr_ret_adr[11] i_csr_ret_adr[10] i_csr_ret_adr[9] i_csr_ret_adr[8] i_csr_ret_adr[7] i_csr_ret_adr[6]
+ i_csr_ret_adr[5] i_csr_ret_adr[4] i_csr_ret_adr[3] i_csr_ret_adr[2] i_csr_ret_adr[1] rv_alu1
x4 net52[31] net52[30] net52[29] net52[28] net52[27] net52[26] net52[25] net52[24] net52[23]
+ net52[22] net52[21] net52[20] net52[19] net52[18] net52[17] net52[16] net52[15] net52[14] net52[13] net52[12]
+ net52[11] net52[10] net52[9] net52[8] net52[7] net52[6] net52[5] net52[4] net52[3] net52[2] net52[1] net52[0]
+ clk_p[2] reset_n[1] net53[31] net53[30] net53[29] net53[28] net53[27] net53[26] net53[25] net53[24]
+ net53[23] net53[22] net53[21] net53[20] net53[19] net53[18] net53[17] net53[16] net53[15] net53[14] net53[13]
+ net53[12] net53[11] net53[10] net53[9] net53[8] net53[7] net53[6] net53[5] net53[4] net53[3] net53[2]
+ net53[1] net53[0] net35 net37 net3[4] net3[3] net3[2] net3[1] net3[0] net4[4] net4[3] net4[2] net4[1]
+ net4[0] net40[4] net40[3] net40[2] net40[1] net40[0] net54[31] net54[30] net54[29] net54[28] net54[27]
+ net54[26] net54[25] net54[24] net54[23] net54[22] net54[21] net54[20] net54[19] net54[18] net54[17] net54[16]
+ net54[15] net54[14] net54[13] net54[12] net54[11] net54[10] net54[9] net54[8] net54[7] net54[6] net54[5]
+ net54[4] net54[3] net54[2] net54[1] net54[0] rv_regs
x5 clk_p[0] o_reg_rdata1[31] o_reg_rdata1[30] o_reg_rdata1[29] o_reg_rdata1[28] o_reg_rdata1[27]
+ o_reg_rdata1[26] o_reg_rdata1[25] o_reg_rdata1[24] o_reg_rdata1[23] o_reg_rdata1[22] o_reg_rdata1[21]
+ o_reg_rdata1[20] o_reg_rdata1[19] o_reg_rdata1[18] o_reg_rdata1[17] o_reg_rdata1[16] o_reg_rdata1[15]
+ o_reg_rdata1[14] o_reg_rdata1[13] o_reg_rdata1[12] o_reg_rdata1[11] o_reg_rdata1[10] o_reg_rdata1[9] o_reg_rdata1[8]
+ o_reg_rdata1[7] o_reg_rdata1[6] o_reg_rdata1[5] o_reg_rdata1[4] o_reg_rdata1[3] o_reg_rdata1[2] o_reg_rdata1[1]
+ o_reg_rdata1[0] net33[4] net33[3] net33[2] net33[1] net33[0] net18[31] net18[30] net18[29] net18[28] net18[27]
+ net18[26] net18[25] net18[24] net18[23] net18[22] net18[21] net18[20] net18[19] net18[18] net18[17] net18[16]
+ net18[15] net18[14] net18[13] net18[12] net18[11] net18[10] net18[9] net18[8] net18[7] net18[6] net18[5]
+ net18[4] net18[3] net18[2] net18[1] net18[0] net32[4] net32[3] net32[2] net32[1] net32[0] net41[31]
+ net41[30] net41[29] net41[28] net41[27] net41[26] net41[25] net41[24] net41[23] net41[22] net41[21] net41[20]
+ net41[19] net41[18] net41[17] net41[16] net41[15] net41[14] net41[13] net41[12] net41[11] net41[10] net41[9]
+ net41[8] net41[7] net41[6] net41[5] net41[4] net41[3] net41[2] net41[1] net41[0] net36[4] net36[3] net36[2]
+ net36[1] net36[0] net54[31] net54[30] net54[29] net54[28] net54[27] net54[26] net54[25] net54[24] net54[23]
+ net54[22] net54[21] net54[20] net54[19] net54[18] net54[17] net54[16] net54[15] net54[14] net54[13] net54[12]
+ net54[11] net54[10] net54[9] net54[8] net54[7] net54[6] net54[5] net54[4] net54[3] net54[2] net54[1] net54[0]
+ net40[4] net40[3] net40[2] net40[1] net40[0] net46[31] net46[30] net46[29] net46[28] net46[27] net46[26]
+ net46[25] net46[24] net46[23] net46[22] net46[21] net46[20] net46[19] net46[18] net46[17] net46[16] net46[15]
+ net46[14] net46[13] net46[12] net46[11] net46[10] net46[9] net46[8] net46[7] net46[6] net46[5] net46[4]
+ net46[3] net46[2] net46[1] net46[0] net37 net39 net52[31] net52[30] net52[29] net52[28] net52[27] net52[26]
+ net52[25] net52[24] net52[23] net52[22] net52[21] net52[20] net52[19] net52[18] net52[17] net52[16] net52[15]
+ net52[14] net52[13] net52[12] net52[11] net52[10] net52[9] net52[8] net52[7] net52[6] net52[5] net52[4]
+ net52[3] net52[2] net52[1] net52[0] net53[31] net53[30] net53[29] net53[28] net53[27] net53[26] net53[25]
+ net53[24] net53[23] net53[22] net53[21] net53[20] net53[19] net53[18] net53[17] net53[16] net53[15] net53[14]
+ net53[13] net53[12] net53[11] net53[10] net53[9] net53[8] net53[7] net53[6] net53[5] net53[4] net53[3]
+ net53[2] net53[1] net53[0] net42[31] net42[30] net42[29] net42[28] net42[27] net42[26] net42[25] net42[24]
+ net42[23] net42[22] net42[21] net42[20] net42[19] net42[18] net42[17] net42[16] net42[15] net42[14] net42[13]
+ net42[12] net42[11] net42[10] net42[9] net42[8] net42[7] net42[6] net42[5] net42[4] net42[3] net42[2]
+ net42[1] net42[0] net43[31] net43[30] net43[29] net43[28] net43[27] net43[26] net43[25] net43[24] net43[23]
+ net43[22] net43[21] net43[20] net43[19] net43[18] net43[17] net43[16] net43[15] net43[14] net43[13] net43[12]
+ net43[11] net43[10] net43[9] net43[8] net43[7] net43[6] net43[5] net43[4] net43[3] net43[2] net43[1] net43[0]
+ rv_hazard
x6 alu2_pc_select clk_p[1] reset_n[0] net42[31] net42[30] net42[29] net42[28] net42[27] net42[26]
+ net42[25] net42[24] net42[23] net42[22] net42[21] net42[20] net42[19] net42[18] net42[17] net42[16] net42[15]
+ net42[14] net42[13] net42[12] net42[11] net42[10] net42[9] net42[8] net42[7] net42[6] net42[5] net42[4]
+ net42[3] net42[2] net42[1] net42[0] net19[31] net19[30] net19[29] net19[28] net19[27] net19[26] net19[25]
+ net19[24] net19[23] net19[22] net19[21] net19[20] net19[19] net19[18] net19[17] net19[16] net19[15] net19[14]
+ net19[13] net19[12] net19[11] net19[10] net19[9] net19[8] net19[7] net19[6] net19[5] net19[4] net19[3]
+ net19[2] net19[1] net19[0] o_data_adr[31] o_data_adr[30] o_data_adr[29] o_data_adr[28] o_data_adr[27]
+ o_data_adr[26] o_data_adr[25] o_data_adr[24] o_data_adr[23] o_data_adr[22] o_data_adr[21] o_data_adr[20]
+ o_data_adr[19] o_data_adr[18] o_data_adr[17] o_data_adr[16] o_data_adr[15] o_data_adr[14] o_data_adr[13]
+ o_data_adr[12] o_data_adr[11] o_data_adr[10] o_data_adr[9] o_data_adr[8] o_data_adr[7] o_data_adr[6] o_data_adr[5]
+ o_data_adr[4] o_data_adr[3] o_data_adr[2] o_data_adr[1] o_data_adr[0] o_data_write net20[31] net20[30] net20[29]
+ net20[28] net20[27] net20[26] net20[25] net20[24] net20[23] net20[22] net20[21] net20[20] net20[19] net20[18]
+ net20[17] net20[16] net20[15] net20[14] net20[13] net20[12] net20[11] net20[10] net20[9] net20[8] net20[7]
+ net20[6] net20[5] net20[4] net20[3] net20[2] net20[1] net20[0] net37 net21 net36[4] net36[3] net36[2]
+ net36[1] net36[0] net22 net23[4] net23[3] net23[2] net23[1] net23[0] alu2_pc_target[31] alu2_pc_target[30]
+ alu2_pc_target[29] alu2_pc_target[28] alu2_pc_target[27] alu2_pc_target[26] alu2_pc_target[25] alu2_pc_target[24]
+ alu2_pc_target[23] alu2_pc_target[22] alu2_pc_target[21] alu2_pc_target[20] alu2_pc_target[19] alu2_pc_target[18]
+ alu2_pc_target[17] alu2_pc_target[16] alu2_pc_target[15] alu2_pc_target[14] alu2_pc_target[13] alu2_pc_target[12]
+ alu2_pc_target[11] alu2_pc_target[10] alu2_pc_target[9] alu2_pc_target[8] alu2_pc_target[7] alu2_pc_target[6]
+ alu2_pc_target[5] alu2_pc_target[4] alu2_pc_target[3] alu2_pc_target[2] alu2_pc_target[1] alu2_res_src[2]
+ alu2_res_src[1] alu2_res_src[0] net24 net25 o_data_wdata[31] o_data_wdata[30] o_data_wdata[29] o_data_wdata[28]
+ o_data_wdata[27] o_data_wdata[26] o_data_wdata[25] o_data_wdata[24] o_data_wdata[23] o_data_wdata[22]
+ o_data_wdata[21] o_data_wdata[20] o_data_wdata[19] o_data_wdata[18] o_data_wdata[17] o_data_wdata[16]
+ o_data_wdata[15] o_data_wdata[14] o_data_wdata[13] o_data_wdata[12] o_data_wdata[11] o_data_wdata[10]
+ o_data_wdata[9] o_data_wdata[8] o_data_wdata[7] o_data_wdata[6] o_data_wdata[5] o_data_wdata[4] o_data_wdata[3]
+ o_data_wdata[2] o_data_wdata[1] o_data_wdata[0] o_data_sel[3] o_data_sel[2] o_data_sel[1] o_data_sel[0] net26[30]
+ net26[29] net26[28] net26[27] net26[26] net26[25] net26[24] net26[23] net26[22] net26[21] net26[20] net26[19]
+ net26[18] net26[17] net26[16] net26[15] net26[14] net26[13] net26[12] net26[11] net26[10] net26[9] net26[8]
+ net26[7] net26[6] net26[5] net26[4] net26[3] net26[2] net26[1] net26[0] net27[30] net27[29] net27[28]
+ net27[27] net27[26] net27[25] net27[24] net27[23] net27[22] net27[21] net27[20] net27[19] net27[18] net27[17]
+ net27[16] net27[15] net27[14] net27[13] net27[12] net27[11] net27[10] net27[9] net27[8] net27[7] net27[6]
+ net27[5] net27[4] net27[3] net27[2] net27[1] net27[0] net38[2] net38[1] net38[0] alu2_to_trap net28[30]
+ net28[29] net28[28] net28[27] net28[26] net28[25] net28[24] net28[23] net28[22] net28[21] net28[20] net28[19]
+ net28[18] net28[17] net28[16] net28[15] net28[14] net28[13] net28[12] net28[11] net28[10] net28[9] net28[8]
+ net28[7] net28[6] net28[5] net28[4] net28[3] net28[2] net28[1] net28[0] alu1_res_src[2] alu1_res_src[1]
+ alu1_res_src[0] net35 net29[2] net29[1] net29[0] net30[4] net30[3] net30[2] net30[1] net30[0] net31 net46[31]
+ net46[30] net46[29] net46[28] net46[27] net46[26] net46[25] net46[24] net46[23] net46[22] net46[21] net46[20]
+ net46[19] net46[18] net46[17] net46[16] net46[15] net46[14] net46[13] net46[12] net46[11] net46[10] net46[9]
+ net46[8] net46[7] net46[6] net46[5] net46[4] net46[3] net46[2] net46[1] net46[0] i_csr_read i_csr_data[31]
+ i_csr_data[30] i_csr_data[29] i_csr_data[28] i_csr_data[27] i_csr_data[26] i_csr_data[25] i_csr_data[24]
+ i_csr_data[23] i_csr_data[22] i_csr_data[21] i_csr_data[20] i_csr_data[19] i_csr_data[18] i_csr_data[17]
+ i_csr_data[16] i_csr_data[15] i_csr_data[14] i_csr_data[13] i_csr_data[12] i_csr_data[11] i_csr_data[10]
+ i_csr_data[9] i_csr_data[8] i_csr_data[7] i_csr_data[6] i_csr_data[5] i_csr_data[4] i_csr_data[3] i_csr_data[2]
+ i_csr_data[1] i_csr_data[0] net50 rv_alu2
x7 clk_p[1] net39 net38[2] net38[1] net38[0] net43[31] net43[30] net43[29] net43[28] net43[27]
+ net43[26] net43[25] net43[24] net43[23] net43[22] net43[21] net43[20] net43[19] net43[18] net43[17] net43[16]
+ net43[15] net43[14] net43[13] net43[12] net43[11] net43[10] net43[9] net43[8] net43[7] net43[6] net43[5]
+ net43[4] net43[3] net43[2] net43[1] net43[0] net41[31] net41[30] net41[29] net41[28] net41[27] net41[26]
+ net41[25] net41[24] net41[23] net41[22] net41[21] net41[20] net41[19] net41[18] net41[17] net41[16] net41[15]
+ net41[14] net41[13] net41[12] net41[11] net41[10] net41[9] net41[8] net41[7] net41[6] net41[5] net41[4]
+ net41[3] net41[2] net41[1] net41[0] net40[4] net40[3] net40[2] net40[1] net40[0] net37 net36[4] net36[3]
+ net36[2] net36[1] net36[0] alu2_res_src[2] i_data_rdata[31] i_data_rdata[30] i_data_rdata[29]
+ i_data_rdata[28] i_data_rdata[27] i_data_rdata[26] i_data_rdata[25] i_data_rdata[24] i_data_rdata[23]
+ i_data_rdata[22] i_data_rdata[21] i_data_rdata[20] i_data_rdata[19] i_data_rdata[18] i_data_rdata[17]
+ i_data_rdata[16] i_data_rdata[15] i_data_rdata[14] i_data_rdata[13] i_data_rdata[12] i_data_rdata[11]
+ i_data_rdata[10] i_data_rdata[9] i_data_rdata[8] i_data_rdata[7] i_data_rdata[6] i_data_rdata[5] i_data_rdata[4]
+ i_data_rdata[3] i_data_rdata[2] i_data_rdata[1] i_data_rdata[0] net34 rv_write
x200 net35 VSS VSS VCC VCC net34 sky130_fd_sc_hs__inv_1
x201 alu2_res_src[2] o_data_write VSS VSS VCC VCC o_data_req sky130_fd_sc_hs__or2_1
x202 o_data_req net37 VSS VSS VCC VCC o_instr_issued sky130_fd_sc_hs__or2_1
* noconn i_data_ack
x8 clk_p[2] net51 reset_n[1] o_csr_masked net49 fetch_pc_change net48 net44 net47 net35
+ alu1_res_src[2] net50 net55 net56 net3[4] net3[3] net3[2] net3[1] net3[0] net4[4] net4[3] net4[2] net4[1] net4[0]
+ net23[4] net23[3] net23[2] net23[1] net23[0] rv_ctrl
x9 net25 net24 net45 VSS VSS VCC VCC net56 sky130_fd_sc_hs__o21a_1
* noconn #net55
**.ends
.end
